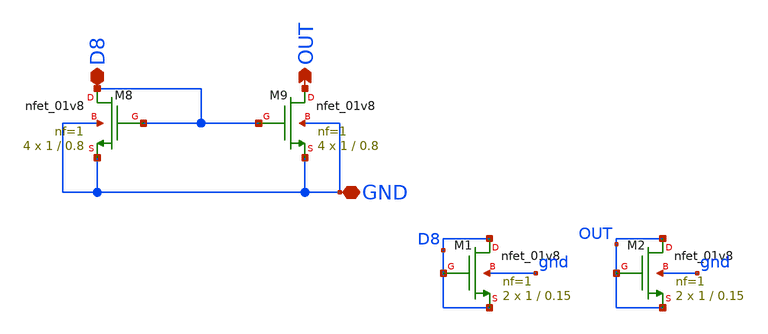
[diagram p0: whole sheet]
** sch_path: opamp/mag/nmos89.sch
**.subckt nmos89 GND D8 OUT
*.iopin GND
*.iopin D8
*.opin OUT
XM8 D8 D8 GND GND sky130_fd_pr__nfet_01v8 L=0.8 W=1 nf=1 ad='int((nf+1)/2) * W/nf * 0.29' as='int((nf+2)/2) * W/nf * 0.29'
+ pd='2*int((nf+1)/2) * (W/nf + 0.29)' ps='2*int((nf+2)/2) * (W/nf + 0.29)' nrd='0.29 / W' nrs='0.29 / W'
+ sa=0 sb=0 sd=0 mult=4 m=4
XM9 OUT D8 GND GND sky130_fd_pr__nfet_01v8 L=0.8 W=1 nf=1 ad='int((nf+1)/2) * W/nf * 0.29' as='int((nf+2)/2) * W/nf * 0.29'
+ pd='2*int((nf+1)/2) * (W/nf + 0.29)' ps='2*int((nf+2)/2) * (W/nf + 0.29)' nrd='0.29 / W' nrs='0.29 / W'
+ sa=0 sb=0 sd=0 mult=4 m=4
XM1 D8 D8 D8 gnd sky130_fd_pr__nfet_01v8 L=0.15 W=1 nf=1 ad='int((nf+1)/2) * W/nf * 0.29' as='int((nf+2)/2) * W/nf * 0.29'
+ pd='2*int((nf+1)/2) * (W/nf + 0.29)' ps='2*int((nf+2)/2) * (W/nf + 0.29)' nrd='0.29 / W' nrs='0.29 / W'
+ sa=0 sb=0 sd=0 mult=2 m=2
XM2 OUT OUT OUT gnd sky130_fd_pr__nfet_01v8 L=0.15 W=1 nf=1 ad='int((nf+1)/2) * W/nf * 0.29' as='int((nf+2)/2) * W/nf * 0.29'
+ pd='2*int((nf+1)/2) * (W/nf + 0.29)' ps='2*int((nf+2)/2) * (W/nf + 0.29)' nrd='0.29 / W' nrs='0.29 / W'
+ sa=0 sb=0 sd=0 mult=2 m=2
**.ends
.end
